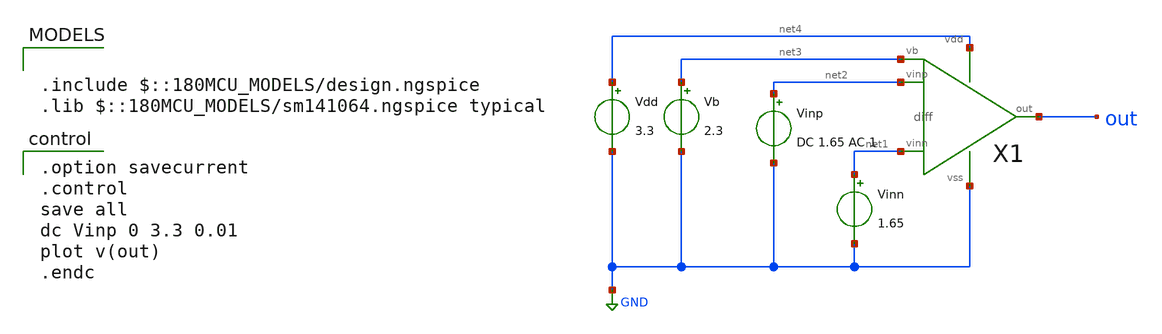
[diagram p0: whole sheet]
** sch_path: opamp/diff_dc.sch
**.subckt diff_dc
Vdd net4 GND 3.3
Vb net3 GND 2.3
Vinn net1 GND 1.65
Vinp net2 GND DC 1.65 AC 1
X1 net2 net1 out net4 GND net3 diff
**** begin user architecture code

.include $::180MCU_MODELS/design.ngspice
.lib $::180MCU_MODELS/sm141064.ngspice typical


.option savecurrent
.control
save all
dc Vinp 0 3.3 0.01
plot v(out)
.endc

**** end user architecture code
**.ends
.GLOBAL GND
.end
